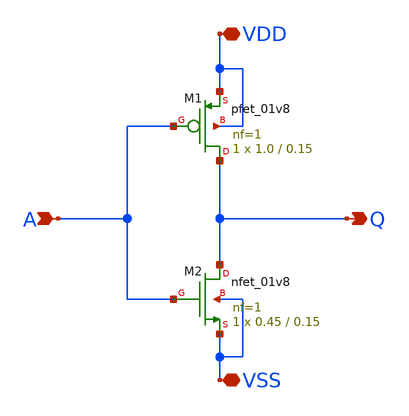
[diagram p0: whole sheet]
** sch_path: samples/inverter/SKY130/inverter.sch
**.subckt inverter Q A VDD VSS
*.opin Q
*.ipin A
*.iopin VDD
*.iopin VSS
XM2 Q A VSS VSS sky130_fd_pr__nfet_01v8 L=0.15 W=0.45 nf=1 ad='int((1 + 1)/2) * 0.45 / 1 * 0.29' as='int((1 + 2)/2) * 0.45 / 1 * 0.29'
+ pd='2*int((1 + 1)/2) * (0.45 / 1 + 0.29)' ps='2*int((1 + 2)/2) * (0.45 / 1 + 0.29)' nrd='0.29 / 0.45 '
+ nrs='0.29 / 0.45 ' sa=0 sb=0 sd=0 mult=1 m=1
XM1 Q A VDD VDD sky130_fd_pr__pfet_01v8 L=0.15 W=1.0 nf=1 ad='int((1 + 1)/2) * 1.0 / 1 * 0.29' as='int((1 + 2)/2) * 1.0 / 1 * 0.29'
+ pd='2*int((1 + 1)/2) * (1.0 / 1 + 0.29)' ps='2*int((1 + 2)/2) * (1.0 / 1 + 0.29)' nrd='0.29 / 1.0 ' nrs='0.29 / 1.0 '
+ sa=0 sb=0 sd=0 mult=1 m=1
**.ends
.end
